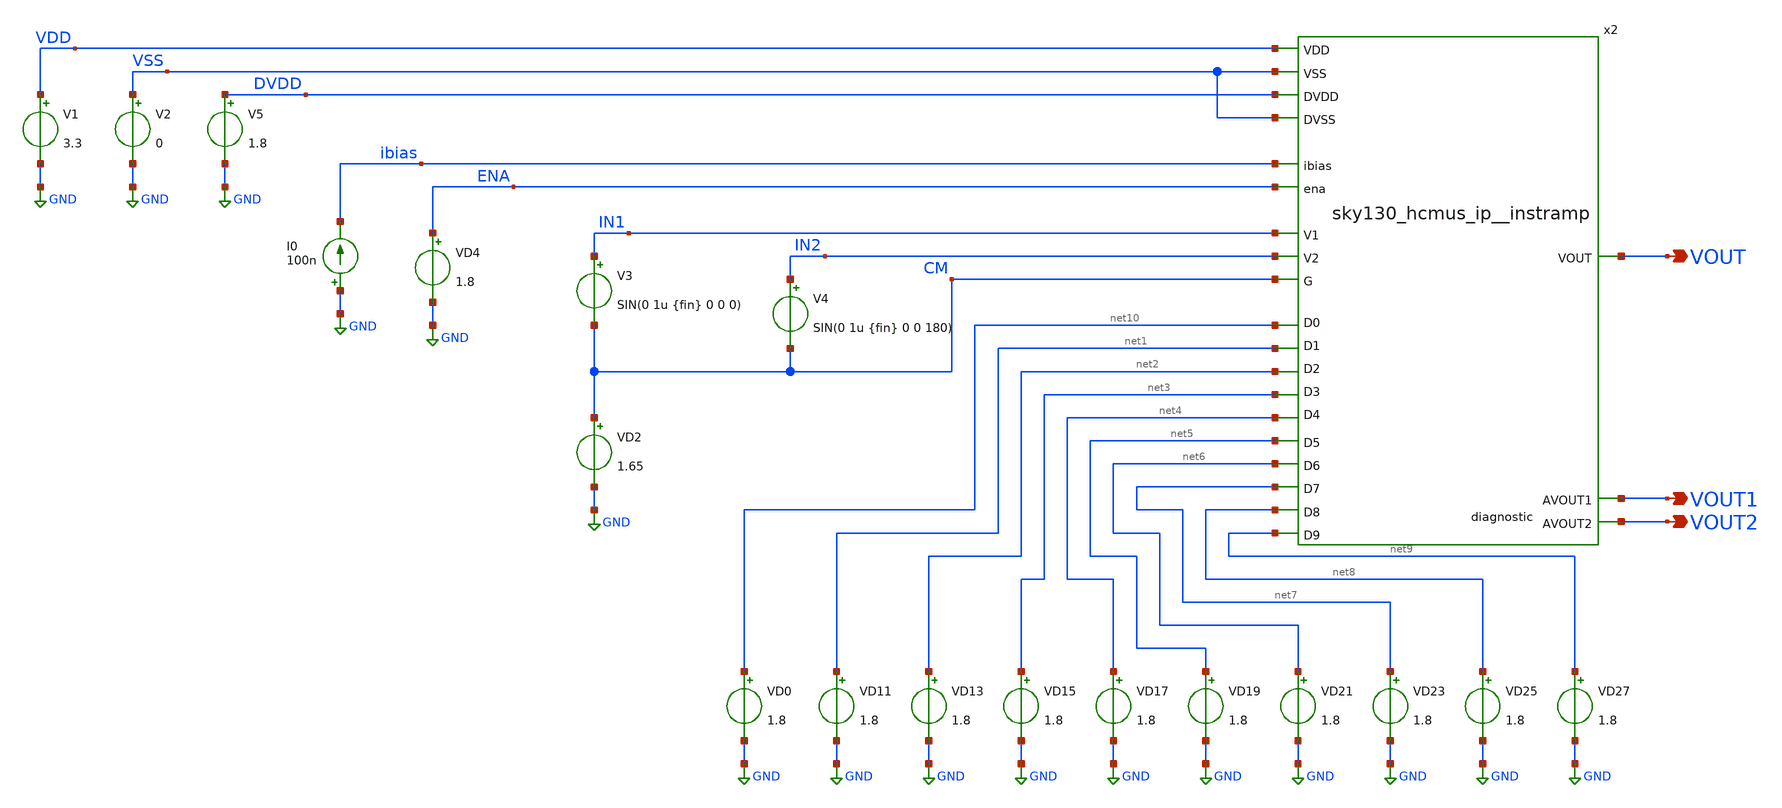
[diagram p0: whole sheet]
** sch_path: xschem/sky130_hcmus_ip__instramp_tb.sch
**.subckt sky130_hcmus_ip__instramp_tb VOUT VOUT1 VOUT2
*.opin VOUT
*.opin VOUT1
*.opin VOUT2
V1 VDD GND 3.3
V2 VSS GND 0
V3 IN1 CM SIN(0 1u {fin} 0 0 0)
V4 IN2 CM SIN(0 1u {fin} 0 0 180)
VD0 net10 GND 1.8
VD11 net1 GND 1.8
VD13 net2 GND 1.8
VD15 net3 GND 1.8
VD17 net4 GND 1.8
VD19 net5 GND 1.8
VD21 net6 GND 1.8
VD23 net7 GND 1.8
VD25 net8 GND 1.8
VD27 net9 GND 1.8
x2 VDD VSS CM IN1 IN2 net10 net1 net2 net3 net4 net5 net6 net7 net8 net9 VOUT1 VOUT2 VOUT ibias ENA
+ DVDD VSS sky130_hcmus_ip__instramp
I0 GND ibias 100n
VD2 CM GND 1.65
VD4 ENA GND 1.8
V5 DVDD GND 1.8
**** begin user architecture code

* Instrumentation amplifier testbench
.lib /usr/share/pdk/sky130A/libs.tech/ngspice/sky130.lib.spice tt
*.include ../netlist/layout/sky130_hcmus_ip__instramp.spice
.include /usr/share/pdk/sky130A/libs.ref/sky130_fd_sc_hvl/spice/sky130_fd_sc_hvl.spice
.param fin = 10K
.control
save all
tran 0.1u 100u
meas tran minv MIN v(vout)
meas tran maxv MAX v(vout)
let gain = ((abs(maxv)+abs(minv))/(2e-6))
print gain
write sky130_hcmus_ip__instramp_tb.raw
.endc

**** end user architecture code
**.ends
.GLOBAL GND
.end
